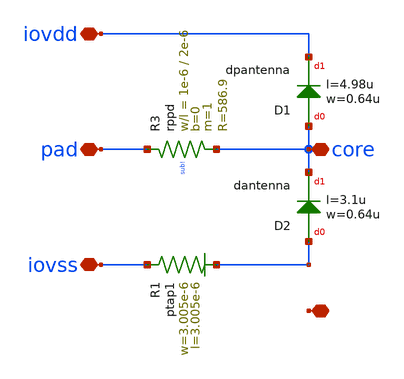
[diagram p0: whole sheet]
** sch_path: ihp-sg13g2/sg13g2_io/xschem/sg13g2_SecondaryProtection.sch
**.subckt sg13g2_SecondaryProtection iovss core pad iovdd !
*.iopin iovss
*.iopin core
*.iopin pad
*.iopin iovdd
*.iopin !
XR1 iovss ! ptap1 R=46.56 w=3.005e-6 l=3.005e-6
XD1 core iovdd dpantenna l=4.98u w=0.64u
XD2 ! core dantenna l=3.1u w=0.64u
XR3 pad core sub! rppd w=1e-6 l=2e-6 m=1 b=0 mm_ok=1
**.ends
.end
